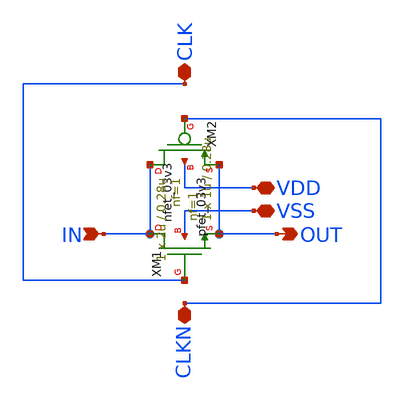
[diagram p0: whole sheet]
** sch_path: CAD6/DFF_Ray/TGATE.sch
**.subckt TGATE IN OUT CLKN CLK VDD VSS
*.ipin IN
*.opin OUT
*.iopin CLKN
*.iopin CLK
*.iopin VDD
*.iopin VSS
XM1 IN CLK OUT VSS nfet_03v3 L=0.28u W=1u nf=1 ad='int((nf+1)/2) * W/nf * 0.18u' as='int((nf+2)/2) * W/nf * 0.18u'
+ pd='2*int((nf+1)/2) * (W/nf + 0.18u)' ps='2*int((nf+2)/2) * (W/nf + 0.18u)' nrd='0.18u / W' nrs='0.18u / W'
+ sa=0 sb=0 sd=0 m=1
XM2 IN CLKN OUT VDD pfet_03v3 L=0.28u W=2u nf=1 ad='int((nf+1)/2) * W/nf * 0.18u' as='int((nf+2)/2) * W/nf * 0.18u'
+ pd='2*int((nf+1)/2) * (W/nf + 0.18u)' ps='2*int((nf+2)/2) * (W/nf + 0.18u)' nrd='0.18u / W' nrs='0.18u / W'
+ sa=0 sb=0 sd=0 m=1
**.ends
.end
